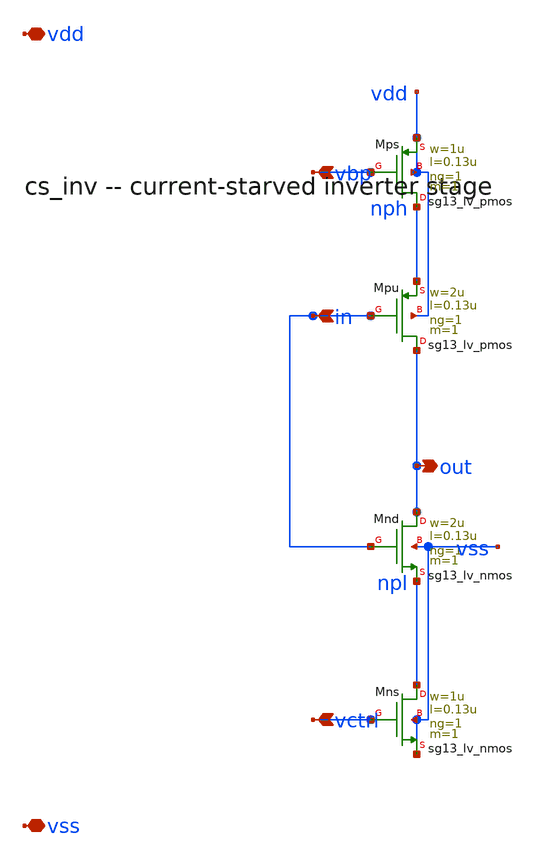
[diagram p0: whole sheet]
** sch_path: xschem/cs_inv_wired.sch
**.subckt cs_inv_wired in out vbp vctrl vdd vss
*.ipin in
*.opin out
*.ipin vbp
*.ipin vctrl
*.iopin vdd
*.iopin vss
XMps nph vbp vdd vdd sg13_lv_pmos w=1u l=0.13u ng=1 m=1 mm_ok=1
XMpu out in nph vdd sg13_lv_pmos w=2u l=0.13u ng=1 m=1 mm_ok=1
XMnd out in npl vss sg13_lv_nmos w=2u l=0.13u ng=1 m=1 mm_ok=1
XMns npl vctrl vss vss sg13_lv_nmos w=1u l=0.13u ng=1 m=1 mm_ok=1
**.ends
.end
